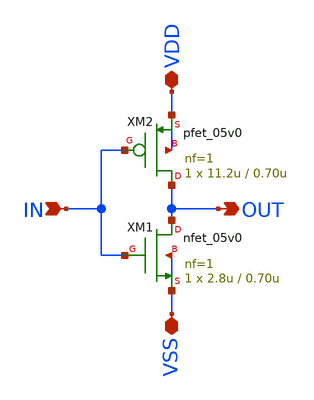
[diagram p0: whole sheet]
** sch_path: design/schematics/CCIA/Non_Overlapping_clk_gen/SG_B11_cic_bms_afe_inv_2x.sch
**.subckt SG_B11_cic_bms_afe_inv_2x IN VDD VSS OUT
*.ipin IN
*.iopin VDD
*.iopin VSS
*.opin OUT
XM1 OUT IN VSS VSS nfet_05v0 L=0.70u W=2.8u nf=1 ad='int((nf+1)/2) * W/nf * 0.18u' as='int((nf+2)/2) * W/nf * 0.18u'
+ pd='2*int((nf+1)/2) * (W/nf + 0.18u)' ps='2*int((nf+2)/2) * (W/nf + 0.18u)' nrd='0.18u / W' nrs='0.18u / W'
+ sa=0 sb=0 sd=0 m=1
XM2 OUT IN VDD VDD pfet_05v0 L=0.70u W=11.2u nf=1 ad='int((nf+1)/2) * W/nf * 0.18u' as='int((nf+2)/2) * W/nf * 0.18u'
+ pd='2*int((nf+1)/2) * (W/nf + 0.18u)' ps='2*int((nf+2)/2) * (W/nf + 0.18u)' nrd='0.18u / W' nrs='0.18u / W'
+ sa=0 sb=0 sd=0 m=1
**.ends
.end
